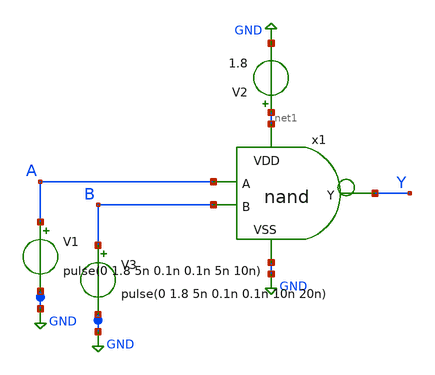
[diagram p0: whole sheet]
** sch_path: Layouts and Schematics/Spice Sim and Schem/nandtest.sch
**.subckt nandtest
V1 A GND pulse(0 1.8 5n 0.1n 0.1n 5n 10n)
V2 net1 GND 1.8
x1 net1 A Y B GND nand
V3 B GND pulse(0 1.8 5n 0.1n 0.1n 10n 20n)
**** begin user architecture code
 .lib $::SKYWATER_MODELS/sky130.lib.spice tt

.tran 1n 40n
.control
run
.endc

**** end user architecture code
**.ends

* expanding   symbol:  nand.sym # of pins=5
** sym_path: Layouts and Schematics/Spice Sim and Schem/nand.sym
** sch_path: Layouts and Schematics/Spice Sim and Schem/nand.sch
.subckt nand VDD A Y B VSS
*.ipin A
*.ipin B
*.ipin VSS
*.opin Y
*.ipin VDD
XM1 Y B net1 VSS sky130_fd_pr__nfet_01v8 L=0.5 W=2 nf=1 ad='int((nf+1)/2) * W/nf * 0.29' as='int((nf+2)/2) * W/nf * 0.29'
+ pd='2*int((nf+1)/2) * (W/nf + 0.29)' ps='2*int((nf+2)/2) * (W/nf + 0.29)' nrd='0.29 / W' nrs='0.29 / W'
+ sa=0 sb=0 sd=0 mult=1 m=1
XM3 Y B VDD VDD sky130_fd_pr__pfet_01v8 L=0.5 W=2 nf=1 ad='int((nf+1)/2) * W/nf * 0.29' as='int((nf+2)/2) * W/nf * 0.29'
+ pd='2*int((nf+1)/2) * (W/nf + 0.29)' ps='2*int((nf+2)/2) * (W/nf + 0.29)' nrd='0.29 / W' nrs='0.29 / W'
+ sa=0 sb=0 sd=0 mult=1 m=1
XM4 Y A VDD VDD sky130_fd_pr__pfet_01v8 L=0.5 W=2 nf=1 ad='int((nf+1)/2) * W/nf * 0.29' as='int((nf+2)/2) * W/nf * 0.29'
+ pd='2*int((nf+1)/2) * (W/nf + 0.29)' ps='2*int((nf+2)/2) * (W/nf + 0.29)' nrd='0.29 / W' nrs='0.29 / W'
+ sa=0 sb=0 sd=0 mult=1 m=1
XM2 net1 A VSS VSS sky130_fd_pr__nfet_01v8 L=0.5 W=2 nf=1 ad='int((nf+1)/2) * W/nf * 0.29' as='int((nf+2)/2) * W/nf * 0.29'
+ pd='2*int((nf+1)/2) * (W/nf + 0.29)' ps='2*int((nf+2)/2) * (W/nf + 0.29)' nrd='0.29 / W' nrs='0.29 / W'
+ sa=0 sb=0 sd=0 mult=1 m=1
.ends

.GLOBAL GND
.end
